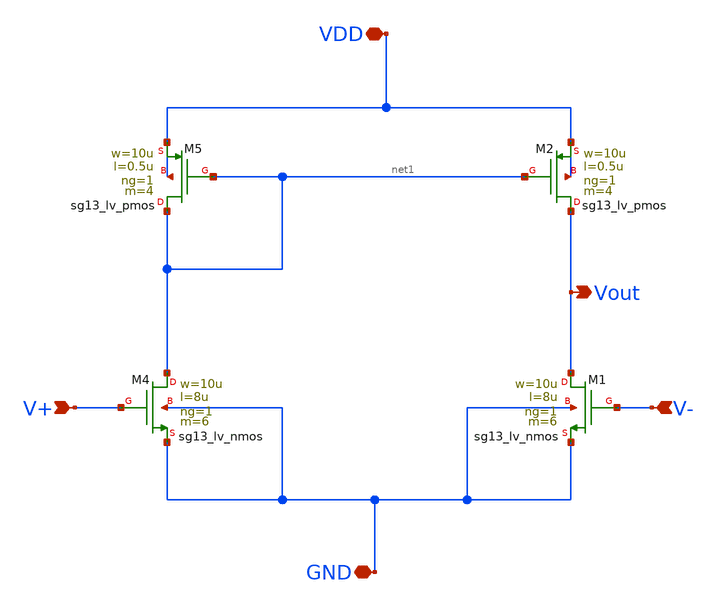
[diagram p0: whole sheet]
** sch_path: SSDOR_w_startup_1V_ihp/Ib_4u/Ib_4u_opamp/Ib_4u_opamp.sch
**.subckt Ib_4u_opamp VDD V+ V- GND Vout
*.iopin VDD
*.ipin V+
*.ipin V-
*.iopin GND
*.opin Vout
XM4 net1 V+ GND GND sg13_lv_nmos w=10u l=8u ng=1 m=6 mm_ok=1
XM5 net1 net1 VDD VDD sg13_lv_pmos w=10u l=0.5u ng=1 m=4 mm_ok=1
XM2 Vout net1 VDD VDD sg13_lv_pmos w=10u l=0.5u ng=1 m=4 mm_ok=1
XM1 Vout V- GND GND sg13_lv_nmos w=10u l=8u ng=1 m=6 mm_ok=1
**.ends
.end
